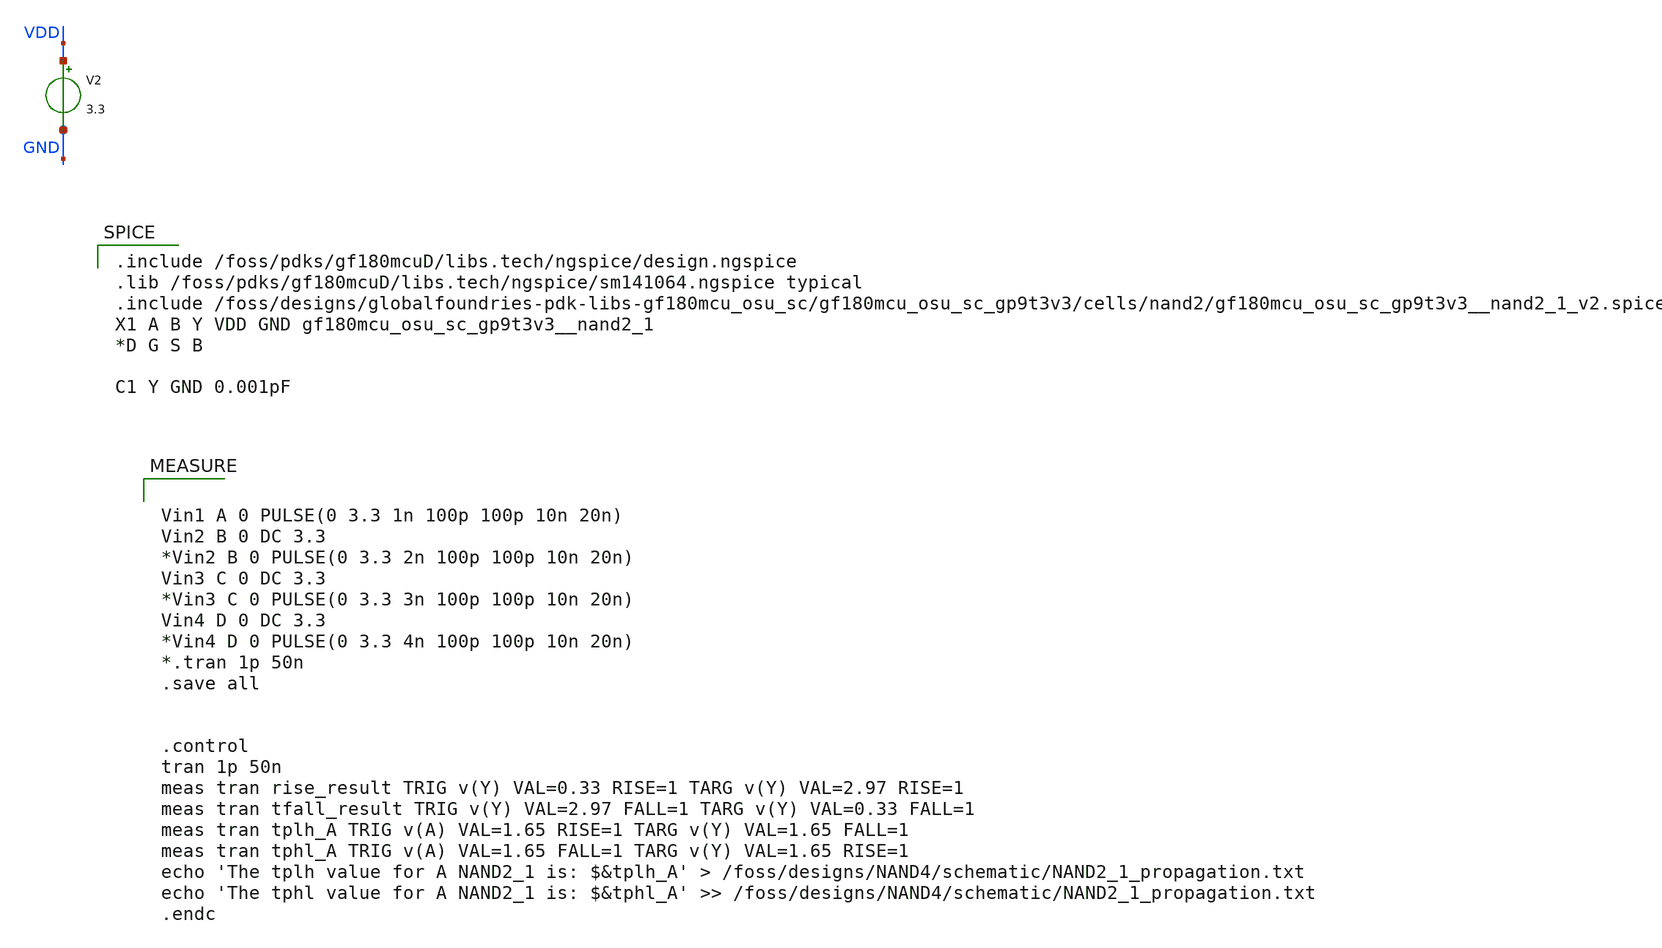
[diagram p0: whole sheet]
** sch_path: designs/libs/tb_archive/existingSC_Test/NAND2_1_char.sch
**.subckt NAND2_1_char
V2 VDD GND 3.3
**** begin user architecture code

.include /foss/pdks/gf180mcuD/libs.tech/ngspice/design.ngspice
.lib /foss/pdks/gf180mcuD/libs.tech/ngspice/sm141064.ngspice typical
.include /foss/designs/globalfoundries-pdk-libs-gf180mcu_osu_sc/gf180mcu_osu_sc_gp9t3v3/cells/nand2/gf180mcu_osu_sc_gp9t3v3__nand2_1_v2.spice
X1 A B Y VDD GND gf180mcu_osu_sc_gp9t3v3__nand2_1
*D G S B

C1 Y GND 0.001pF






Vin1 A 0 PULSE(0 3.3 1n 100p 100p 10n 20n)
Vin2 B 0 DC 3.3
*Vin2 B 0 PULSE(0 3.3 2n 100p 100p 10n 20n)
Vin3 C 0 DC 3.3
*Vin3 C 0 PULSE(0 3.3 3n 100p 100p 10n 20n)
Vin4 D 0 DC 3.3
*Vin4 D 0 PULSE(0 3.3 4n 100p 100p 10n 20n)
*.tran 1p 50n
.save all


.control
tran 1p 50n
meas tran rise_result TRIG v(Y) VAL=0.33 RISE=1 TARG v(Y) VAL=2.97 RISE=1
meas tran tfall_result TRIG v(Y) VAL=2.97 FALL=1 TARG v(Y) VAL=0.33 FALL=1
meas tran tplh_A TRIG v(A) VAL=1.65 RISE=1 TARG v(Y) VAL=1.65 FALL=1
meas tran tphl_A TRIG v(A) VAL=1.65 FALL=1 TARG v(Y) VAL=1.65 RISE=1
echo 'The tplh value for A NAND2_1 is: $&tplh_A' > /foss/designs/NAND4/schematic/NAND2_1_propagation.txt
echo 'The tphl value for A NAND2_1 is: $&tphl_A' >> /foss/designs/NAND4/schematic/NAND2_1_propagation.txt
.endc



**** end user architecture code
**.ends
.end
